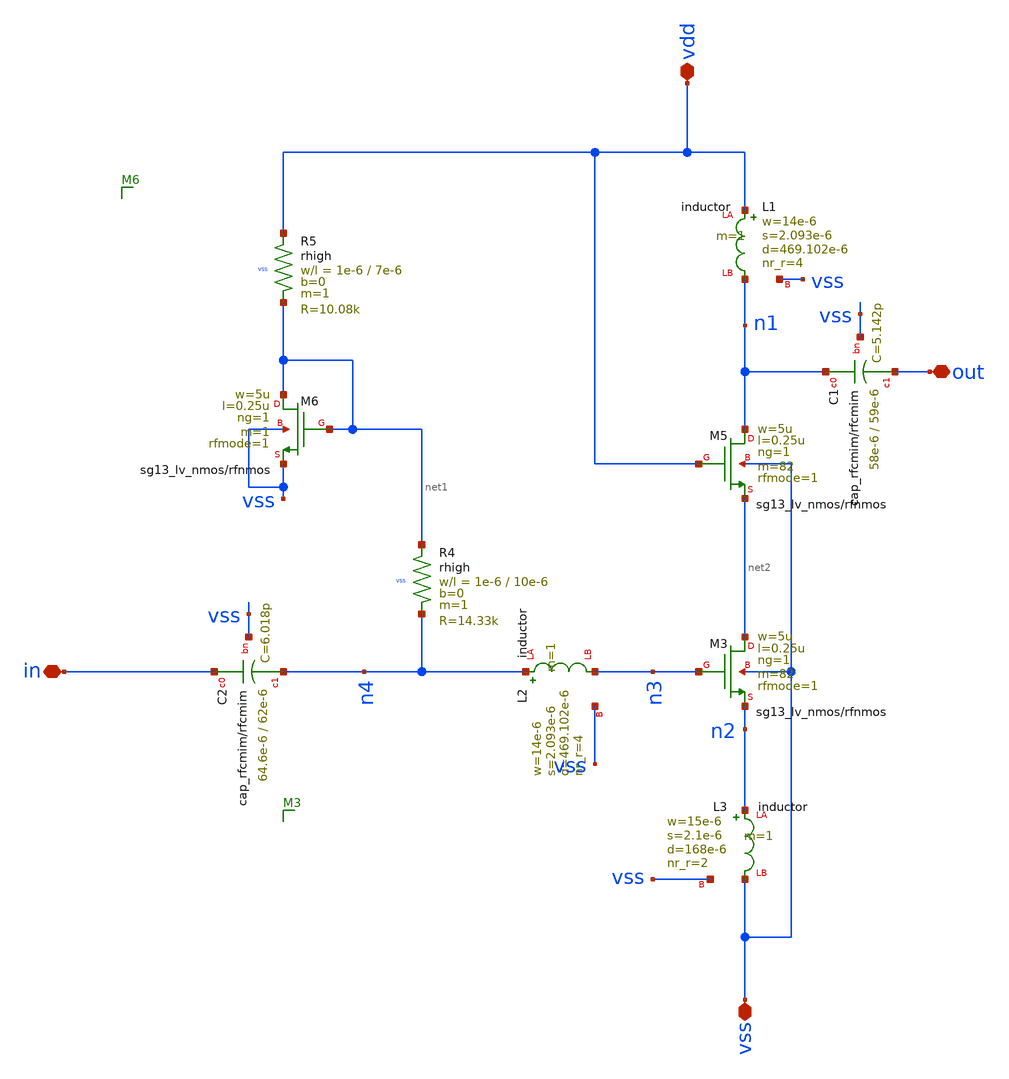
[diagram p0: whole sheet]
** sch_path: LNA7096-main/schematic/xschem/01_lna/LNA_no_buff.sch
**.subckt LNA_no_buff vdd vss in out
*.iopin vdd
*.iopin vss
*.iopin in
*.iopin out
XR4 net1 n4 vss rhigh w=1e-6 l=10e-6 m=1 b=0 mm_ok=1
XR5 vdd net1 vss rhigh w=1e-6 l=7e-6 m=1 b=0 mm_ok=1
XC1 n1 out vss cap_rfcmim w=58e-6 l=59e-6 wfeed=3.0e-6 m=1 mm_ok=1
XM3 net2 n3 n2 vss sg13_lv_nmos w=5u l=0.25u ng=1 m=82 rfmode=1 mm_ok=1
XM5 n1 vdd net2 vss sg13_lv_nmos w=5u l=0.25u ng=1 m=82 rfmode=1 mm_ok=1
XM6 net1 net1 vss vss sg13_lv_nmos w=5u l=0.25u ng=1 m=1 rfmode=1 mm_ok=1
XC2 in n4 vss cap_rfcmim w=64.6e-6 l=62e-6 wfeed=3.0e-6 m=1 mm_ok=1
XL1 vdd n1 vss inductor w=14e-6 s=2.093e-6 d=469.102e-6 nr_r=4 m=1
XL2 n4 n3 vss inductor w=14e-6 s=2.093e-6 d=469.102e-6 nr_r=4 m=1
XL3 n2 vss vss inductor w=15e-6 s=2.1e-6 d=168e-6 nr_r=2 m=1
**.ends
.end
